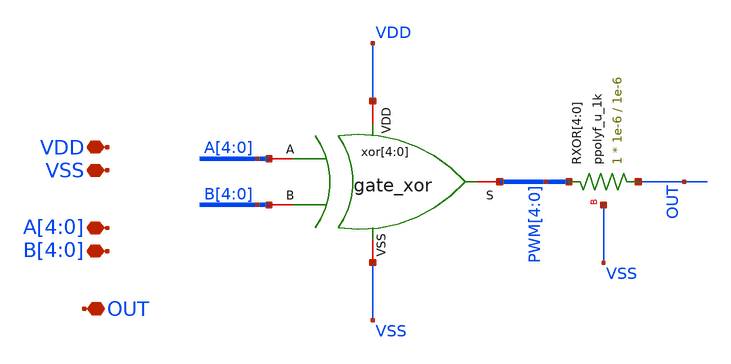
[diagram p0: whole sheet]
** sch_path: designs/integrator_phasedetector/xschem/integrator_phasedetector.sch
**.subckt integrator_phasedetector VDD OUT VSS A[4],A[3],A[2],A[1],A[0] B[4],B[3],B[2],B[1],B[0]
*.iopin VDD
*.iopin OUT
*.iopin VSS
*.iopin A[4],A[3],A[2],A[1],A[0]
*.iopin B[4],B[3],B[2],B[1],B[0]
xor[4] VDD PWM[4] A[4] B[4] VSS gate_xor
xor[3] VDD PWM[3] A[3] B[3] VSS gate_xor
xor[2] VDD PWM[2] A[2] B[2] VSS gate_xor
xor[1] VDD PWM[1] A[1] B[1] VSS gate_xor
xor[0] VDD PWM[0] A[0] B[0] VSS gate_xor
XRXOR[4] OUT PWM[4] VSS ppolyf_u_1k r_width=1e-6 r_length=1e-6 m=1
XRXOR[3] OUT PWM[3] VSS ppolyf_u_1k r_width=1e-6 r_length=1e-6 m=1
XRXOR[2] OUT PWM[2] VSS ppolyf_u_1k r_width=1e-6 r_length=1e-6 m=1
XRXOR[1] OUT PWM[1] VSS ppolyf_u_1k r_width=1e-6 r_length=1e-6 m=1
XRXOR[0] OUT PWM[0] VSS ppolyf_u_1k r_width=1e-6 r_length=1e-6 m=1
**.ends

* expanding   symbol:  gf180/gate_xor/xschem/gate_xor.sym # of pins=5
** sym_path: gf180/gate_xor/xschem/gate_xor.sym
** sch_path: gf180/gate_xor/xschem/gate_xor.sch
.subckt gate_xor VDD S A B VSS
*.iopin VSS
*.iopin VDD
*.iopin S
*.iopin A
*.iopin B
XM2 S B vz VSS nfet_03v3 L=0.28u W=1u nf=1 ad='int((nf+1)/2) * W/nf * 0.18u' as='int((nf+2)/2) * W/nf * 0.18u'
+ pd='2*int((nf+1)/2) * (W/nf + 0.18u)' ps='2*int((nf+2)/2) * (W/nf + 0.18u)' nrd='0.18u / W' nrs='0.18u / W'
+ sa=0 sb=0 sd=0 m=4
XM3 S -B vx VDD pfet_03v3 L=0.28u W=3u nf=1 ad='int((nf+1)/2) * W/nf * 0.18u' as='int((nf+2)/2) * W/nf * 0.18u'
+ pd='2*int((nf+1)/2) * (W/nf + 0.18u)' ps='2*int((nf+2)/2) * (W/nf + 0.18u)' nrd='0.18u / W' nrs='0.18u / W'
+ sa=0 sb=0 sd=0 m=4
XM1 vx A VDD VDD pfet_03v3 L=0.28u W=3u nf=1 ad='int((nf+1)/2) * W/nf * 0.18u' as='int((nf+2)/2) * W/nf * 0.18u'
+ pd='2*int((nf+1)/2) * (W/nf + 0.18u)' ps='2*int((nf+2)/2) * (W/nf + 0.18u)' nrd='0.18u / W' nrs='0.18u / W'
+ sa=0 sb=0 sd=0 m=4
XM4 S -B vw VSS nfet_03v3 L=0.28u W=1u nf=1 ad='int((nf+1)/2) * W/nf * 0.18u' as='int((nf+2)/2) * W/nf * 0.18u'
+ pd='2*int((nf+1)/2) * (W/nf + 0.18u)' ps='2*int((nf+2)/2) * (W/nf + 0.18u)' nrd='0.18u / W' nrs='0.18u / W'
+ sa=0 sb=0 sd=0 m=4
XM5 S B vy VDD pfet_03v3 L=0.28u W=3u nf=1 ad='int((nf+1)/2) * W/nf * 0.18u' as='int((nf+2)/2) * W/nf * 0.18u'
+ pd='2*int((nf+1)/2) * (W/nf + 0.18u)' ps='2*int((nf+2)/2) * (W/nf + 0.18u)' nrd='0.18u / W' nrs='0.18u / W'
+ sa=0 sb=0 sd=0 m=4
XM6 vy -A VDD VDD pfet_03v3 L=0.28u W=3u nf=1 ad='int((nf+1)/2) * W/nf * 0.18u' as='int((nf+2)/2) * W/nf * 0.18u'
+ pd='2*int((nf+1)/2) * (W/nf + 0.18u)' ps='2*int((nf+2)/2) * (W/nf + 0.18u)' nrd='0.18u / W' nrs='0.18u / W'
+ sa=0 sb=0 sd=0 m=4
XM7 vz A VSS VSS nfet_03v3 L=0.28u W=1u nf=1 ad='int((nf+1)/2) * W/nf * 0.18u' as='int((nf+2)/2) * W/nf * 0.18u'
+ pd='2*int((nf+1)/2) * (W/nf + 0.18u)' ps='2*int((nf+2)/2) * (W/nf + 0.18u)' nrd='0.18u / W' nrs='0.18u / W'
+ sa=0 sb=0 sd=0 m=4
XM8 vw -A VSS VSS nfet_03v3 L=0.28u W=1u nf=1 ad='int((nf+1)/2) * W/nf * 0.18u' as='int((nf+2)/2) * W/nf * 0.18u'
+ pd='2*int((nf+1)/2) * (W/nf + 0.18u)' ps='2*int((nf+2)/2) * (W/nf + 0.18u)' nrd='0.18u / W' nrs='0.18u / W'
+ sa=0 sb=0 sd=0 m=4
xINVA VDD -A A VSS gate_inv_L0d28
xINVB VDD -B B VSS gate_inv_L0d28
XM10 VDD VDD vx VDD pfet_03v3 L=0.28u W=3u nf=1 ad='int((nf+1)/2) * W/nf * 0.18u' as='int((nf+2)/2) * W/nf * 0.18u'
+ pd='2*int((nf+1)/2) * (W/nf + 0.18u)' ps='2*int((nf+2)/2) * (W/nf + 0.18u)' nrd='0.18u / W' nrs='0.18u / W'
+ sa=0 sb=0 sd=0 m=2
XM11 VDD VDD vy VDD pfet_03v3 L=0.28u W=3u nf=1 ad='int((nf+1)/2) * W/nf * 0.18u' as='int((nf+2)/2) * W/nf * 0.18u'
+ pd='2*int((nf+1)/2) * (W/nf + 0.18u)' ps='2*int((nf+2)/2) * (W/nf + 0.18u)' nrd='0.18u / W' nrs='0.18u / W'
+ sa=0 sb=0 sd=0 m=2
XM13 vz VSS VSS VSS nfet_03v3 L=0.28u W=1u nf=1 ad='int((nf+1)/2) * W/nf * 0.18u' as='int((nf+2)/2) * W/nf * 0.18u'
+ pd='2*int((nf+1)/2) * (W/nf + 0.18u)' ps='2*int((nf+2)/2) * (W/nf + 0.18u)' nrd='0.18u / W' nrs='0.18u / W'
+ sa=0 sb=0 sd=0 m=2
XM14 vw VSS VSS VSS nfet_03v3 L=0.28u W=1u nf=1 ad='int((nf+1)/2) * W/nf * 0.18u' as='int((nf+2)/2) * W/nf * 0.18u'
+ pd='2*int((nf+1)/2) * (W/nf + 0.18u)' ps='2*int((nf+2)/2) * (W/nf + 0.18u)' nrd='0.18u / W' nrs='0.18u / W'
+ sa=0 sb=0 sd=0 m=2
.ends


* expanding   symbol:
*+  /foss/designs/chipathon_2025/designs/gf180/gate_inv_L0d28/xschem/gate_inv_L0d28.sym # of pins=4
** sym_path: /foss/designs/chipathon_2025/designs/gf180/gate_inv_L0d28/xschem/gate_inv_L0d28.sym
** sch_path: /foss/designs/chipathon_2025/designs/gf180/gate_inv_L0d28/xschem/gate_inv_L0d28.sch
.subckt gate_inv_L0d28 VDD B A VSS
*.opin B
*.ipin A
*.iopin VDD
*.iopin VSS
XMN B A VSS VSS nfet_03v3 L=0.28u W=1u nf=1 ad='int((nf+1)/2) * W/nf * 0.18u' as='int((nf+2)/2) * W/nf * 0.18u'
+ pd='2*int((nf+1)/2) * (W/nf + 0.18u)' ps='2*int((nf+2)/2) * (W/nf + 0.18u)' nrd='0.18u / W' nrs='0.18u / W'
+ sa=0 sb=0 sd=0 m=2
XMP B A VDD VDD pfet_03v3 L=0.28u W=3u nf=1 ad='int((nf+1)/2) * W/nf * 0.18u' as='int((nf+2)/2) * W/nf * 0.18u'
+ pd='2*int((nf+1)/2) * (W/nf + 0.18u)' ps='2*int((nf+2)/2) * (W/nf + 0.18u)' nrd='0.18u / W' nrs='0.18u / W'
+ sa=0 sb=0 sd=0 m=2
.ends

.end
